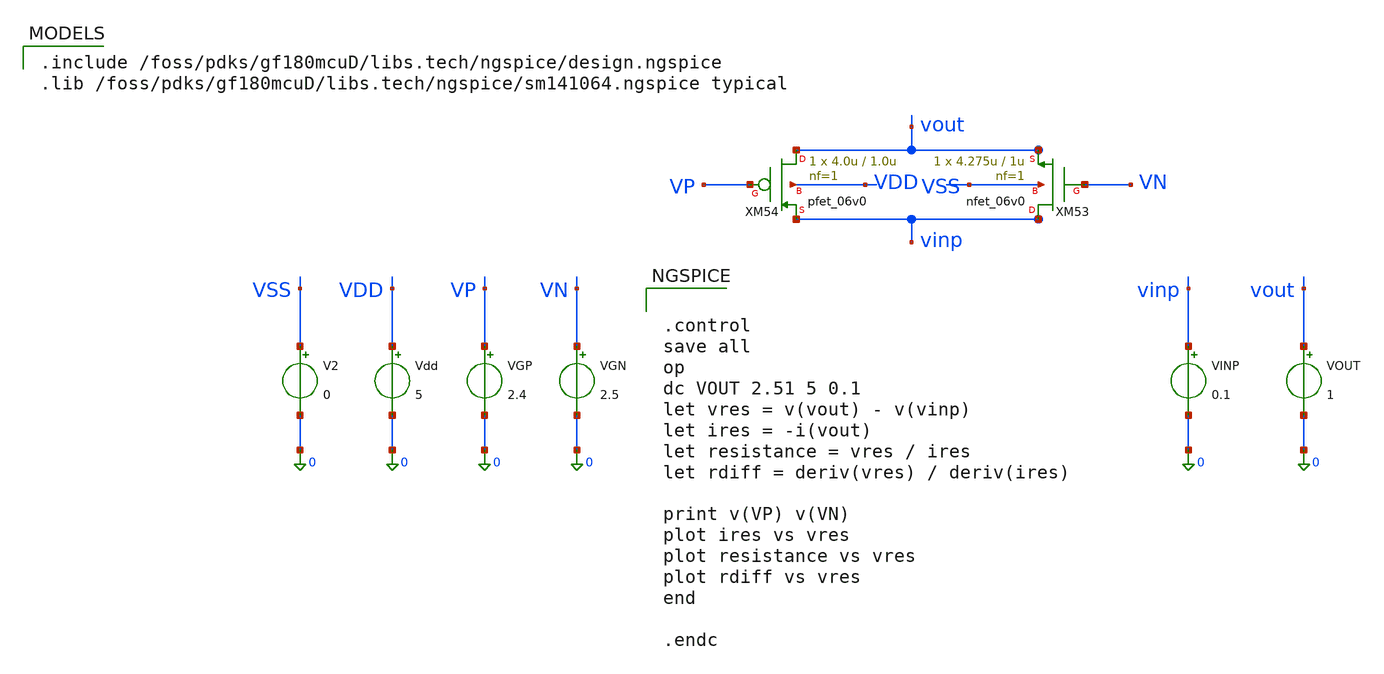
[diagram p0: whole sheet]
** sch_path: activities/opamp3An/RfLinearityCheck.sch
**.subckt RfLinearityCheck
XM53 vinp VN vout VSS nfet_06v0 L=1u W=4.275u nf=1 ad='int((nf+1)/2) * W/nf * 0.18u' as='int((nf+2)/2) * W/nf * 0.18u'
+ pd='2*int((nf+1)/2) * (W/nf + 0.18u)' ps='2*int((nf+2)/2) * (W/nf + 0.18u)' nrd='0.18u / W' nrs='0.18u / W'
+ sa=0 sb=0 sd=0 m=1
XM54 vout VP vinp VDD pfet_06v0 L=1.0u W=4.0u nf=1 ad='int((nf+1)/2) * W/nf * 0.18u' as='int((nf+2)/2) * W/nf * 0.18u'
+ pd='2*int((nf+1)/2) * (W/nf + 0.18u)' ps='2*int((nf+2)/2) * (W/nf + 0.18u)' nrd='0.18u / W' nrs='0.18u / W'
+ sa=0 sb=0 sd=0 m=1
V2 VSS 0 0
Vdd VDD 0 5
VGP VP 0 2.4
VGN VN 0 2.5
VINP vinp 0 0.1
VOUT vout 0 1
**** begin user architecture code

.include /foss/pdks/gf180mcuD/libs.tech/ngspice/design.ngspice
.lib /foss/pdks/gf180mcuD/libs.tech/ngspice/sm141064.ngspice typical



.control
save all
op
dc VOUT 2.51 5 0.1
let vres = v(vout) - v(vinp)
let ires = -i(vout)
let resistance = vres / ires
let rdiff = deriv(vres) / deriv(ires)

print v(VP) v(VN)
plot ires vs vres
plot resistance vs vres
plot rdiff vs vres
end

.endc

**** end user architecture code
**.ends
.end
